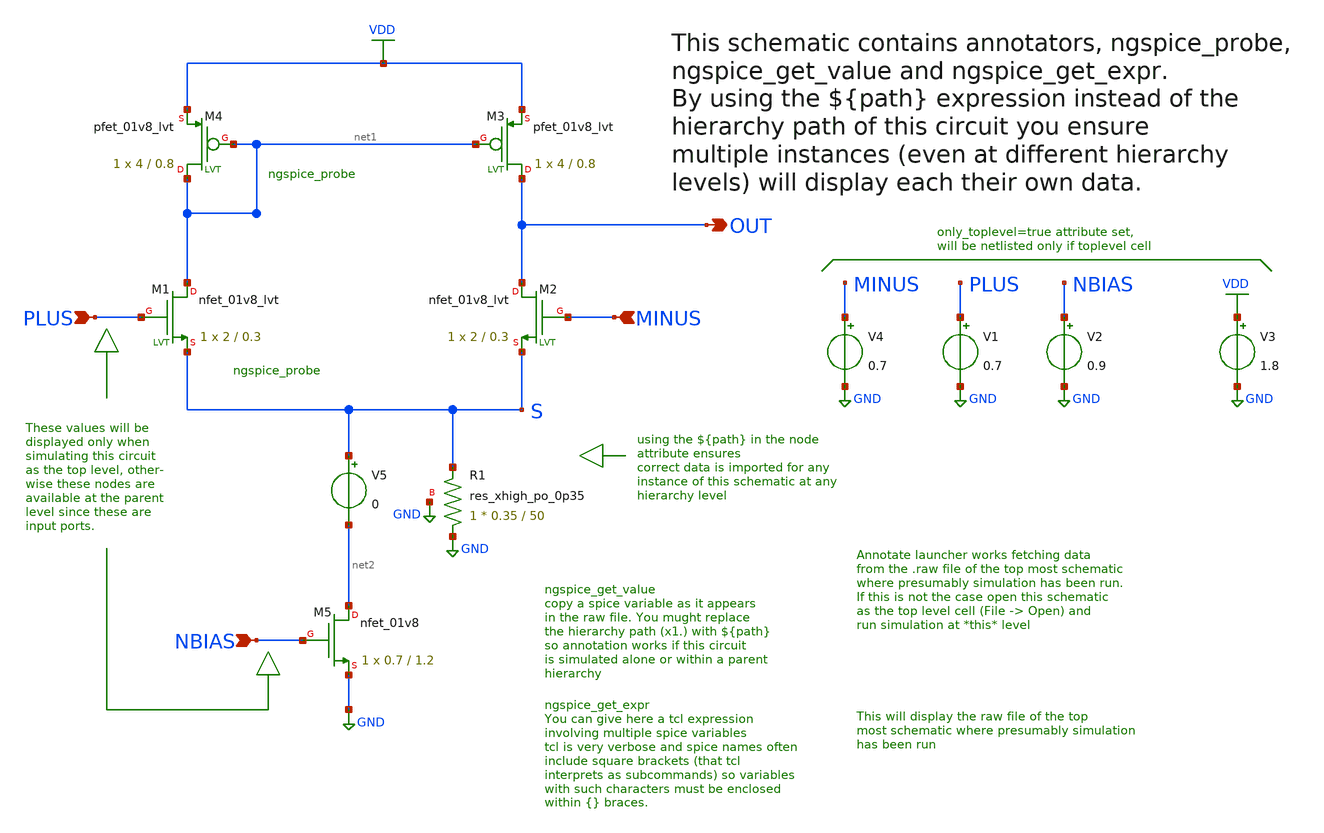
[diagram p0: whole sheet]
** sch_path: xyce/sky130A-xyce/libs.tech/xschem/sky130_tests/n_diffamp.sch
* Copyright 2020 Stefan Frederik Schippers
* Licensed under the Apache License, Version 2.0 (the "License");
* you may not use this file except in compliance with the License.
* You may obtain a copy of the License at
* https://www.apache.org/licenses/LICENSE-2.0
* Unless required by applicable law or agreed to in writing, software
* distributed under the License is distributed on an "AS IS" BASIS,
* WITHOUT WARRANTIES OR CONDITIONS OF ANY KIND, either express or implied.
* See the License for the specific language governing permissions and
* limitations under the License.
**.subckt n_diffamp PLUS MINUS OUT NBIAS
*.ipin PLUS
*.ipin MINUS
*.opin OUT
*.ipin NBIAS
XM1 net1 PLUS S GND sky130_fd_pr__nfet_01v8_lvt L=0.3 W=2 nf=1 ad='int((nf+1)/2) * W/nf * 0.29' as='int((nf+2)/2) * W/nf * 0.29'
+ pd='2*int((nf+1)/2) * (W/nf + 0.29)' ps='2*int((nf+2)/2) * (W/nf + 0.29)' nrd='0.29 / W' nrs='0.29 / W'
+ sa=0 sb=0 sd=0 mult=1 m=1
XM2 OUT MINUS S GND sky130_fd_pr__nfet_01v8_lvt L=0.3 W=2 nf=1 ad='int((nf+1)/2) * W/nf * 0.29' as='int((nf+2)/2) * W/nf * 0.29'
+ pd='2*int((nf+1)/2) * (W/nf + 0.29)' ps='2*int((nf+2)/2) * (W/nf + 0.29)' nrd='0.29 / W' nrs='0.29 / W'
+ sa=0 sb=0 sd=0 mult=1 m=1
XM3 OUT net1 VDD VDD sky130_fd_pr__pfet_01v8_lvt L=0.8 W=4 nf=1 ad='int((nf+1)/2) * W/nf * 0.29' as='int((nf+2)/2) * W/nf * 0.29'
+ pd='2*int((nf+1)/2) * (W/nf + 0.29)' ps='2*int((nf+2)/2) * (W/nf + 0.29)' nrd='0.29 / W' nrs='0.29 / W'
+ sa=0 sb=0 sd=0 mult=1 m=1
XM4 net1 net1 VDD VDD sky130_fd_pr__pfet_01v8_lvt L=0.8 W=4 nf=1 ad='int((nf+1)/2) * W/nf * 0.29' as='int((nf+2)/2) * W/nf * 0.29'
+ pd='2*int((nf+1)/2) * (W/nf + 0.29)' ps='2*int((nf+2)/2) * (W/nf + 0.29)' nrd='0.29 / W' nrs='0.29 / W'
+ sa=0 sb=0 sd=0 mult=1 m=1
XM5 net2 NBIAS GND GND sky130_fd_pr__nfet_01v8 L=1.2 W=0.7 nf=1 ad='int((nf+1)/2) * W/nf * 0.29' as='int((nf+2)/2) * W/nf * 0.29'
+ pd='2*int((nf+1)/2) * (W/nf + 0.29)' ps='2*int((nf+2)/2) * (W/nf + 0.29)' nrd='0.29 / W' nrs='0.29 / W'
+ sa=0 sb=0 sd=0 mult=1 m=1
XR1 GND S GND sky130_fd_pr__res_xhigh_po_0p35 W=0.35 L=50 mult=1 m=1
V1 PLUS GND 0.7
V2 NBIAS GND 0.9
V3 VDD GND 1.8
V4 MINUS GND 0.7
V5 S net2 0
**** begin user architecture code

.include $::SKYWATER_MODELS/cells/nfet_01v8/sky130_fd_pr__nfet_01v8__tt.corner.spice
.include $::SKYWATER_MODELS/cells/nfet_01v8_lvt/sky130_fd_pr__nfet_01v8_lvt__tt.corner.spice
.include $::SKYWATER_MODELS/cells/pfet_01v8/sky130_fd_pr__pfet_01v8__tt.corner.spice
.include $::SKYWATER_MODELS/cells/nfet_03v3_nvt/sky130_fd_pr__nfet_03v3_nvt__tt.corner.spice
.include $::SKYWATER_MODELS/cells/nfet_05v0_nvt/sky130_fd_pr__nfet_05v0_nvt__tt.corner.spice
.include $::SKYWATER_MODELS/cells/esd_nfet_01v8/sky130_fd_pr__esd_nfet_01v8__tt.corner.spice
.include $::SKYWATER_MODELS/cells/pfet_01v8_lvt/sky130_fd_pr__pfet_01v8_lvt__tt.corner.spice
.include $::SKYWATER_MODELS/cells/pfet_01v8_hvt/sky130_fd_pr__pfet_01v8_hvt__tt.corner.spice
.include $::SKYWATER_MODELS/cells/esd_pfet_g5v0d10v5/sky130_fd_pr__esd_pfet_g5v0d10v5__tt.corner.spice
.include $::SKYWATER_MODELS/cells/pfet_g5v0d10v5/sky130_fd_pr__pfet_g5v0d10v5__tt.corner.spice
.include $::SKYWATER_MODELS/cells/pfet_g5v0d16v0/sky130_fd_pr__pfet_g5v0d16v0__tt.corner.spice
.include $::SKYWATER_MODELS/cells/nfet_g5v0d10v5/sky130_fd_pr__nfet_g5v0d10v5__tt.corner.spice
.include $::SKYWATER_MODELS/cells/nfet_g5v0d16v0/sky130_fd_pr__nfet_g5v0d16v0__tt_discrete.corner.spice
.include $::SKYWATER_MODELS/cells/esd_nfet_g5v0d10v5/sky130_fd_pr__esd_nfet_g5v0d10v5__tt.corner.spice
.include $::SKYWATER_MODELS/models/corners/tt/nonfet.spice
* Mismatch parameters
.include $::SKYWATER_MODELS/cells/nfet_01v8/sky130_fd_pr__nfet_01v8__mismatch.corner.spice
.include $::SKYWATER_MODELS/cells/pfet_01v8/sky130_fd_pr__pfet_01v8__mismatch.corner.spice
.include $::SKYWATER_MODELS/cells/nfet_01v8_lvt/sky130_fd_pr__nfet_01v8_lvt__mismatch.corner.spice
.include $::SKYWATER_MODELS/cells/pfet_01v8_lvt/sky130_fd_pr__pfet_01v8_lvt__mismatch.corner.spice
.include $::SKYWATER_MODELS/cells/pfet_01v8_hvt/sky130_fd_pr__pfet_01v8_hvt__mismatch.corner.spice
.include $::SKYWATER_MODELS/cells/nfet_g5v0d10v5/sky130_fd_pr__nfet_g5v0d10v5__mismatch.corner.spice
.include $::SKYWATER_MODELS/cells/pfet_g5v0d10v5/sky130_fd_pr__pfet_g5v0d10v5__mismatch.corner.spice
.include $::SKYWATER_MODELS/cells/nfet_05v0_nvt/sky130_fd_pr__nfet_05v0_nvt__mismatch.corner.spice
.include $::SKYWATER_MODELS/cells/nfet_03v3_nvt/sky130_fd_pr__nfet_03v3_nvt__mismatch.corner.spice
* Resistor$::SKYWATER_MODELS/Capacitor
.include $::SKYWATER_MODELS/models/r+c/res_typical__cap_typical.spice
.include $::SKYWATER_MODELS/models/r+c/res_typical__cap_typical__lin.spice
* Special cells
.include $::SKYWATER_MODELS/models/corners/tt/specialized_cells.spice
* All models
.include $::SKYWATER_MODELS/models/all.spice
* Corner
.include $::SKYWATER_MODELS/models/corners/tt/rf.spice

**** end user architecture code
**.ends
.GLOBAL GND
.GLOBAL VDD
**** begin user architecture code

.options savecurrents
.control
save @m.xm5.msky130_fd_pr__nfet_01v8[gm]
save all
op
write n_diffamp.raw
.endc


**** end user architecture code
.end
